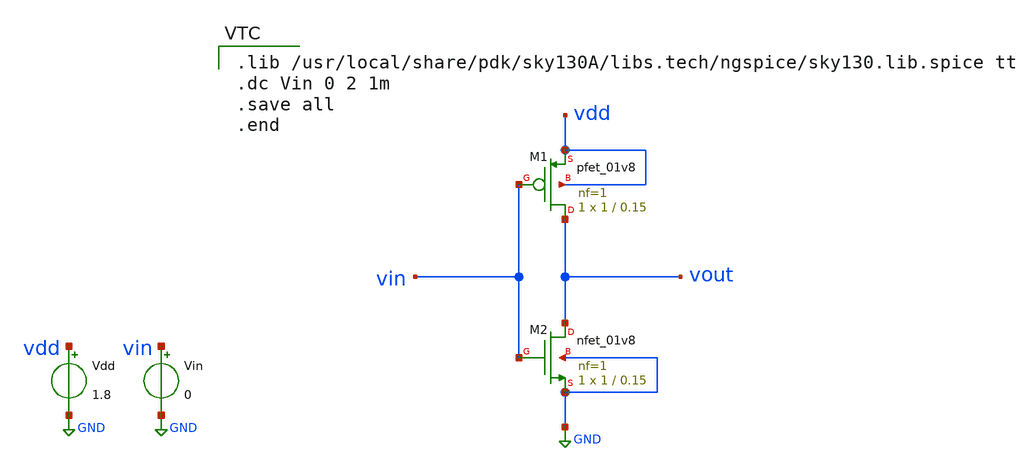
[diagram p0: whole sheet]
** sch_path: inverter_test.sch
**.subckt inverter_test
Vdd vdd GND 1.8
Vin vin GND 0
XM1 vout vin vdd vdd sky130_fd_pr__pfet_01v8 L=0.15 W=1 nf=1 ad='int((1 + 1)/2) * 1 / 1 * 0.29' as='int((1 + 2)/2) * 1 / 1 * 0.29'
+ pd='2*int((1 + 1)/2) * (1 / 1 + 0.29)' ps='2*int((1 + 2)/2) * (1 / 1 + 0.29)' nrd='0.29 / 1 ' nrs='0.29 / 1 '
+ sa=0 sb=0 sd=0 mult=1 m=1
XM2 vout vin GND GND sky130_fd_pr__nfet_01v8 L=0.15 W=1 nf=1 ad='int((1 + 1)/2) * 1 / 1 * 0.29' as='int((1 + 2)/2) * 1 / 1 * 0.29'
+ pd='2*int((1 + 1)/2) * (1 / 1 + 0.29)' ps='2*int((1 + 2)/2) * (1 / 1 + 0.29)' nrd='0.29 / 1 ' nrs='0.29 / 1 '
+ sa=0 sb=0 sd=0 mult=1 m=1
**** begin user architecture code

.lib /usr/local/share/pdk/sky130A/libs.tech/ngspice/sky130.lib.spice tt
.dc Vin 0 2 1m
.save all
.end

**** end user architecture code
**.ends
.GLOBAL GND
.end
